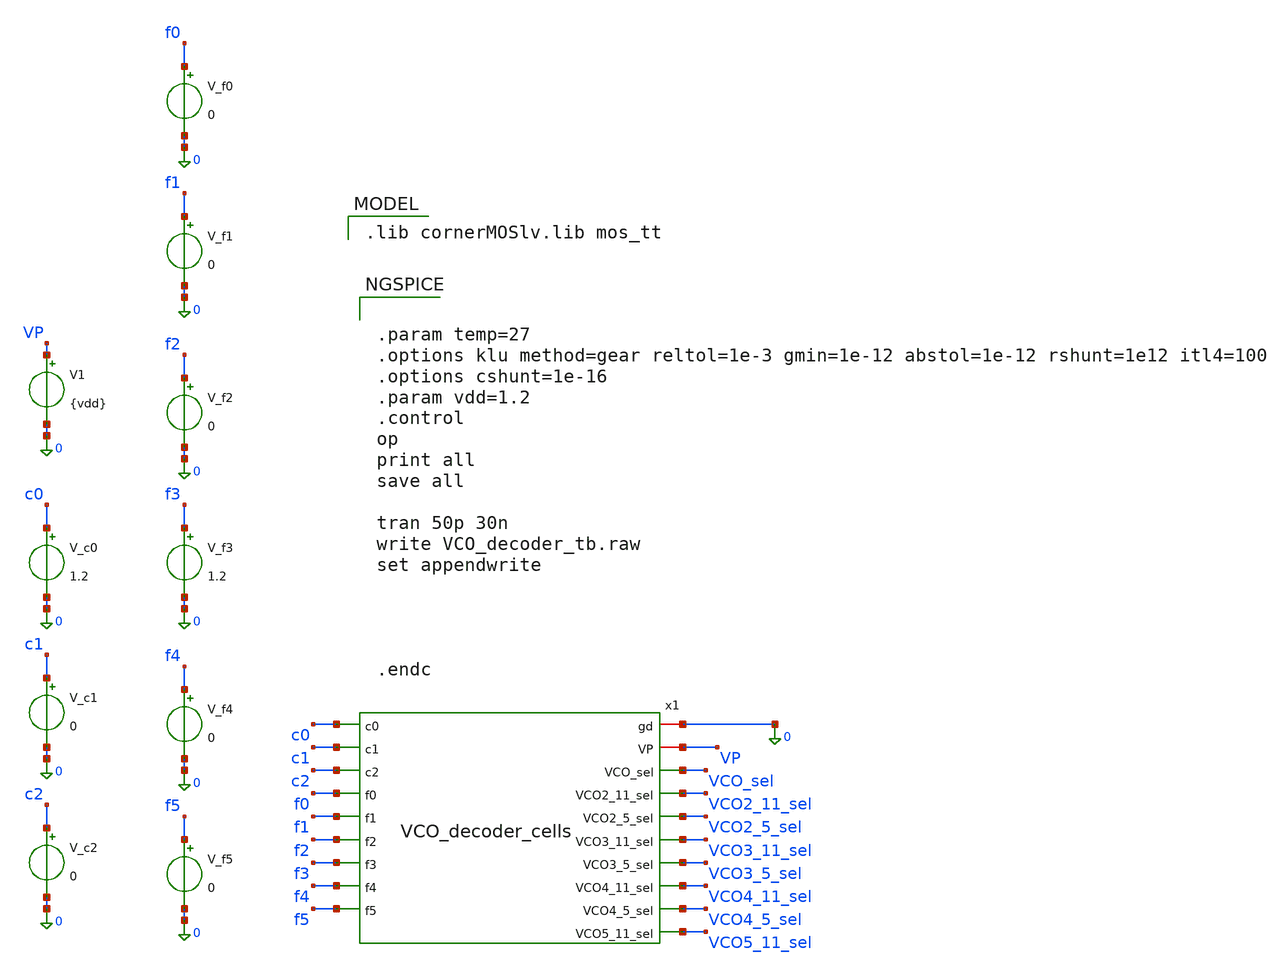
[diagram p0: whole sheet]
** sch_path: PLL0663-main/testbenches/tran/xschem/divider/VCO_decoder_tb_fk.sch
**.subckt VCO_decoder_tb_fk
V1 VP 0 {vdd}
V_c0 c0 0 1.2
V_f1 f1 0 0
V_c1 c1 0 0
V_c2 c2 0 0
V_f0 f0 0 0
x1 0 VP c0 c1 c2 f0 f1 f2 f3 f4 f5 VCO_sel VCO2_11_sel VCO2_5_sel VCO3_11_sel VCO3_5_sel VCO4_11_sel
+ VCO4_5_sel VCO5_11_sel VCO_decoder_cells
V_f3 f3 0 1.2
V_f2 f2 0 0
V_f5 f5 0 0
V_f4 f4 0 0
**** begin user architecture code
 .lib cornerMOSlv.lib mos_tt



.param temp=27
.options klu method=gear reltol=1e-3 gmin=1e-12 abstol=1e-12 rshunt=1e12 itl4=100
.options cshunt=1e-16
.param vdd=1.2
.control
op
print all
save all

tran 50p 30n
write VCO_decoder_tb.raw
set appendwrite




.endc


**** end user architecture code
**.ends
.end
